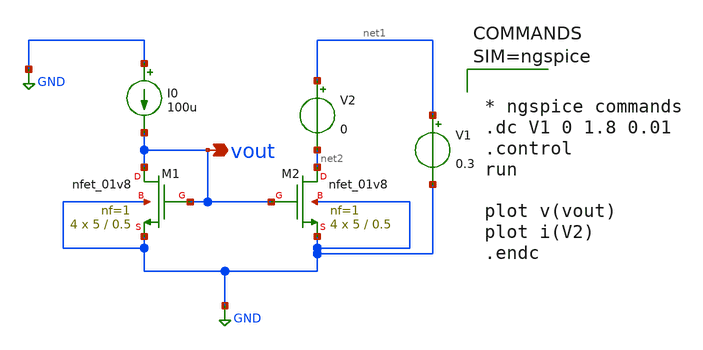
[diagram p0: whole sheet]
** sch_path: xschem/out_imp-case2.sch
**.subckt out_imp-case2 vout
*.opin vout
XM2 net2 vout GND GND sky130_fd_pr__nfet_01v8 L=0.5 W=5 nf=1 ad='int((1 + 1)/2) * 5 / 1 * 0.29' as='int((1 + 2)/2) * 5 / 1 * 0.29'
+ pd='2*int((1 + 1)/2) * (5 / 1 + 0.29)' ps='2*int((1 + 2)/2) * (5 / 1 + 0.29)' nrd='0.29 / 5 ' nrs='0.29 / 5 '
+ sa=0 sb=0 sd=0 mult=4 m=4
XM1 vout vout GND GND sky130_fd_pr__nfet_01v8 L=0.5 W=5 nf=1 ad='int((1 + 1)/2) * 5 / 1 * 0.29' as='int((1 + 2)/2) * 5 / 1 * 0.29'
+ pd='2*int((1 + 1)/2) * (5 / 1 + 0.29)' ps='2*int((1 + 2)/2) * (5 / 1 + 0.29)' nrd='0.29 / 5 ' nrs='0.29 / 5 '
+ sa=0 sb=0 sd=0 mult=4 m=4
I0 GND vout 100u
V1 net1 GND 0.3
V2 net1 net2 0
**** begin user architecture code

** opencircuitdesign pdks install
.lib $::SKYWATER_MODELS/sky130.lib.spice tt




* ngspice commands
.dc V1 0 1.8 0.01
.control
run

plot v(vout)
plot i(V2)
.endc



**** end user architecture code
**.ends
.GLOBAL GND
.end
